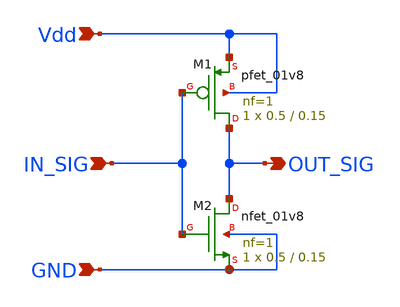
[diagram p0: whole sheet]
** sch_path: latihan_cmos/INVERTER MODULE DIY.sch
**.subckt INVERTER MODULE DIY IN_SIG Vdd GND OUT_SIG
*.ipin IN_SIG
*.ipin Vdd
*.ipin GND
*.opin OUT_SIG
XM1 OUT_SIG IN_SIG Vdd Vdd sky130_fd_pr__pfet_01v8 L=0.15 W=0.5 nf=1 ad='int((nf+1)/2) * W/nf * 0.29'
+ as='int((nf+2)/2) * W/nf * 0.29' pd='2*int((nf+1)/2) * (W/nf + 0.29)' ps='2*int((nf+2)/2) * (W/nf + 0.29)'
+ nrd='0.29 / W' nrs='0.29 / W' sa=0 sb=0 sd=0 mult=1 m=1
XM2 OUT_SIG IN_SIG GND GND sky130_fd_pr__nfet_01v8 L=0.15 W=0.5 nf=1 ad='int((nf+1)/2) * W/nf * 0.29'
+ as='int((nf+2)/2) * W/nf * 0.29' pd='2*int((nf+1)/2) * (W/nf + 0.29)' ps='2*int((nf+2)/2) * (W/nf + 0.29)'
+ nrd='0.29 / W' nrs='0.29 / W' sa=0 sb=0 sd=0 mult=1 m=1
**.ends
.end
